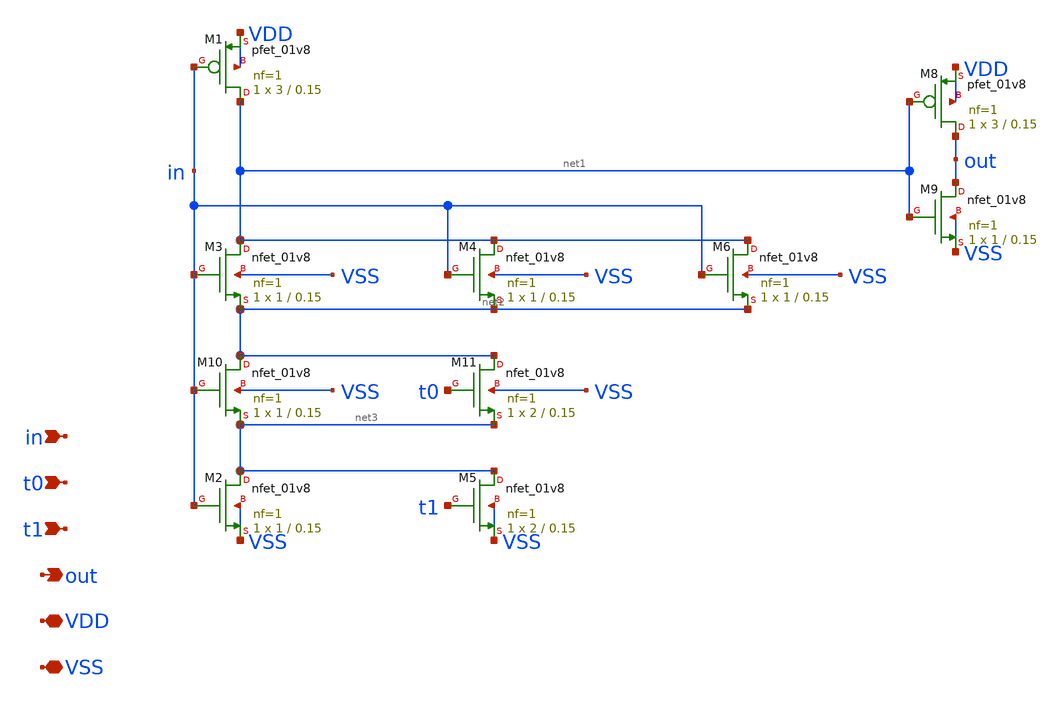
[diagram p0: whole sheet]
** sch_path: xschem/fine_delay.sch
**.subckt fine_delay VDD in out VSS t0 t1
*.iopin VDD
*.ipin in
*.opin out
*.iopin VSS
*.ipin t0
*.ipin t1
XM1 net1 in VDD VDD sky130_fd_pr__pfet_01v8 L=0.15 W=3 nf=1 ad='int((nf+1)/2) * W/nf * 0.29' as='int((nf+2)/2) * W/nf * 0.29'
+ pd='2*int((nf+1)/2) * (W/nf + 0.29)' ps='2*int((nf+2)/2) * (W/nf + 0.29)' nrd='0.29 / W' nrs='0.29 / W'
+ sa=0 sb=0 sd=0 mult=1 m=1
XM2 net3 in VSS VSS sky130_fd_pr__nfet_01v8 L=0.15 W=1 nf=1 ad='int((nf+1)/2) * W/nf * 0.29' as='int((nf+2)/2) * W/nf * 0.29'
+ pd='2*int((nf+1)/2) * (W/nf + 0.29)' ps='2*int((nf+2)/2) * (W/nf + 0.29)' nrd='0.29 / W' nrs='0.29 / W'
+ sa=0 sb=0 sd=0 mult=1 m=1
XM5 net3 t1 VSS VSS sky130_fd_pr__nfet_01v8 L=0.15 W=2 nf=1 ad='int((nf+1)/2) * W/nf * 0.29' as='int((nf+2)/2) * W/nf * 0.29'
+ pd='2*int((nf+1)/2) * (W/nf + 0.29)' ps='2*int((nf+2)/2) * (W/nf + 0.29)' nrd='0.29 / W' nrs='0.29 / W'
+ sa=0 sb=0 sd=0 mult=1 m=1
XM8 out net1 VDD VDD sky130_fd_pr__pfet_01v8 L=0.15 W=3 nf=1 ad='int((nf+1)/2) * W/nf * 0.29' as='int((nf+2)/2) * W/nf * 0.29'
+ pd='2*int((nf+1)/2) * (W/nf + 0.29)' ps='2*int((nf+2)/2) * (W/nf + 0.29)' nrd='0.29 / W' nrs='0.29 / W'
+ sa=0 sb=0 sd=0 mult=1 m=1
XM9 out net1 VSS VSS sky130_fd_pr__nfet_01v8 L=0.15 W=1 nf=1 ad='int((nf+1)/2) * W/nf * 0.29' as='int((nf+2)/2) * W/nf * 0.29'
+ pd='2*int((nf+1)/2) * (W/nf + 0.29)' ps='2*int((nf+2)/2) * (W/nf + 0.29)' nrd='0.29 / W' nrs='0.29 / W'
+ sa=0 sb=0 sd=0 mult=1 m=1
XM10 net2 in net3 VSS sky130_fd_pr__nfet_01v8 L=0.15 W=1 nf=1 ad='int((nf+1)/2) * W/nf * 0.29' as='int((nf+2)/2) * W/nf * 0.29'
+ pd='2*int((nf+1)/2) * (W/nf + 0.29)' ps='2*int((nf+2)/2) * (W/nf + 0.29)' nrd='0.29 / W' nrs='0.29 / W'
+ sa=0 sb=0 sd=0 mult=1 m=1
XM11 net2 t0 net3 VSS sky130_fd_pr__nfet_01v8 L=0.15 W=2 nf=1 ad='int((nf+1)/2) * W/nf * 0.29' as='int((nf+2)/2) * W/nf * 0.29'
+ pd='2*int((nf+1)/2) * (W/nf + 0.29)' ps='2*int((nf+2)/2) * (W/nf + 0.29)' nrd='0.29 / W' nrs='0.29 / W'
+ sa=0 sb=0 sd=0 mult=1 m=1
XM3 net1 in net2 VSS sky130_fd_pr__nfet_01v8 L=0.15 W=1 nf=1 ad='int((nf+1)/2) * W/nf * 0.29' as='int((nf+2)/2) * W/nf * 0.29'
+ pd='2*int((nf+1)/2) * (W/nf + 0.29)' ps='2*int((nf+2)/2) * (W/nf + 0.29)' nrd='0.29 / W' nrs='0.29 / W'
+ sa=0 sb=0 sd=0 mult=1 m=1
XM4 net1 in net2 VSS sky130_fd_pr__nfet_01v8 L=0.15 W=1 nf=1 ad='int((nf+1)/2) * W/nf * 0.29' as='int((nf+2)/2) * W/nf * 0.29'
+ pd='2*int((nf+1)/2) * (W/nf + 0.29)' ps='2*int((nf+2)/2) * (W/nf + 0.29)' nrd='0.29 / W' nrs='0.29 / W'
+ sa=0 sb=0 sd=0 mult=1 m=1
XM6 net1 in net2 VSS sky130_fd_pr__nfet_01v8 L=0.15 W=1 nf=1 ad='int((nf+1)/2) * W/nf * 0.29' as='int((nf+2)/2) * W/nf * 0.29'
+ pd='2*int((nf+1)/2) * (W/nf + 0.29)' ps='2*int((nf+2)/2) * (W/nf + 0.29)' nrd='0.29 / W' nrs='0.29 / W'
+ sa=0 sb=0 sd=0 mult=1 m=1
**.ends
.end
